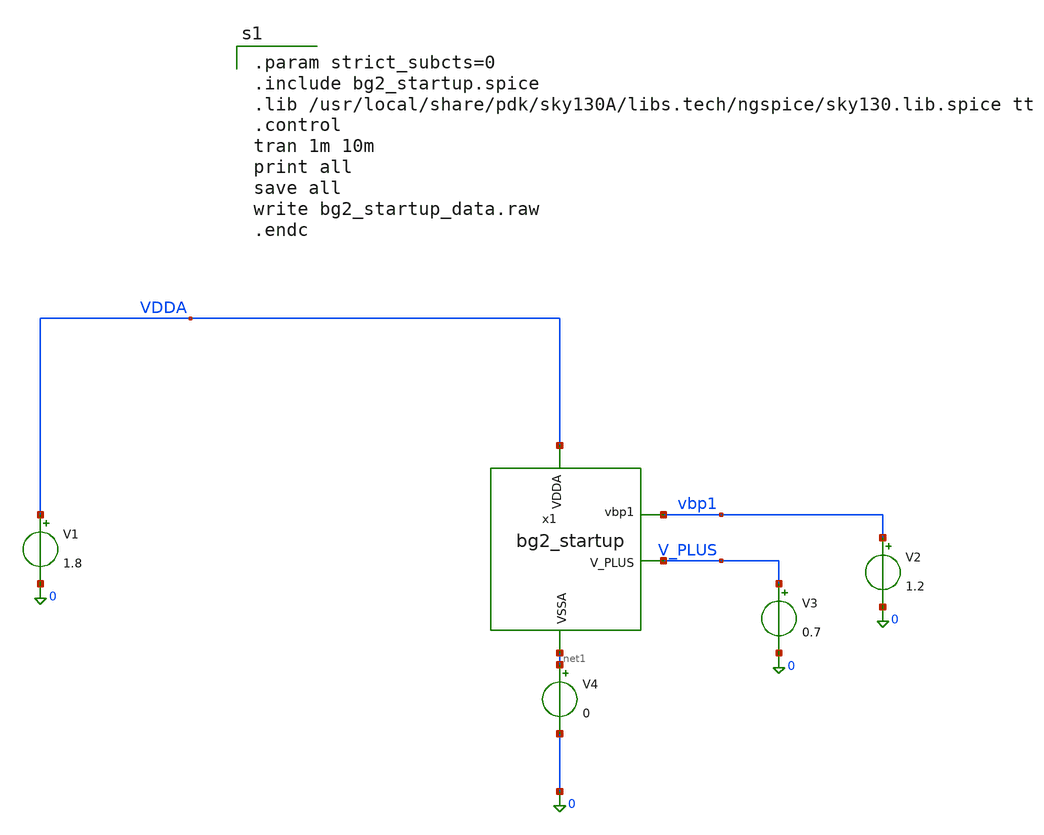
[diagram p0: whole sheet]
** sch_path: lef/bg2_startup_tb.sch
**.subckt bg2_startup_tb
V1 VDDA 0 1.8
V4 net1 0 0
x1 VDDA vbp1 V_PLUS net1 bg2_startup
V2 vbp1 0 1.2
V3 V_PLUS 0 0.7
**** begin user architecture code

.param strict_subcts=0
.include bg2_startup.spice
.lib /usr/local/share/pdk/sky130A/libs.tech/ngspice/sky130.lib.spice tt
.control
tran 1m 10m
print all
save all
write bg2_startup_data.raw
.endc

**** end user architecture code
**.ends
.end
